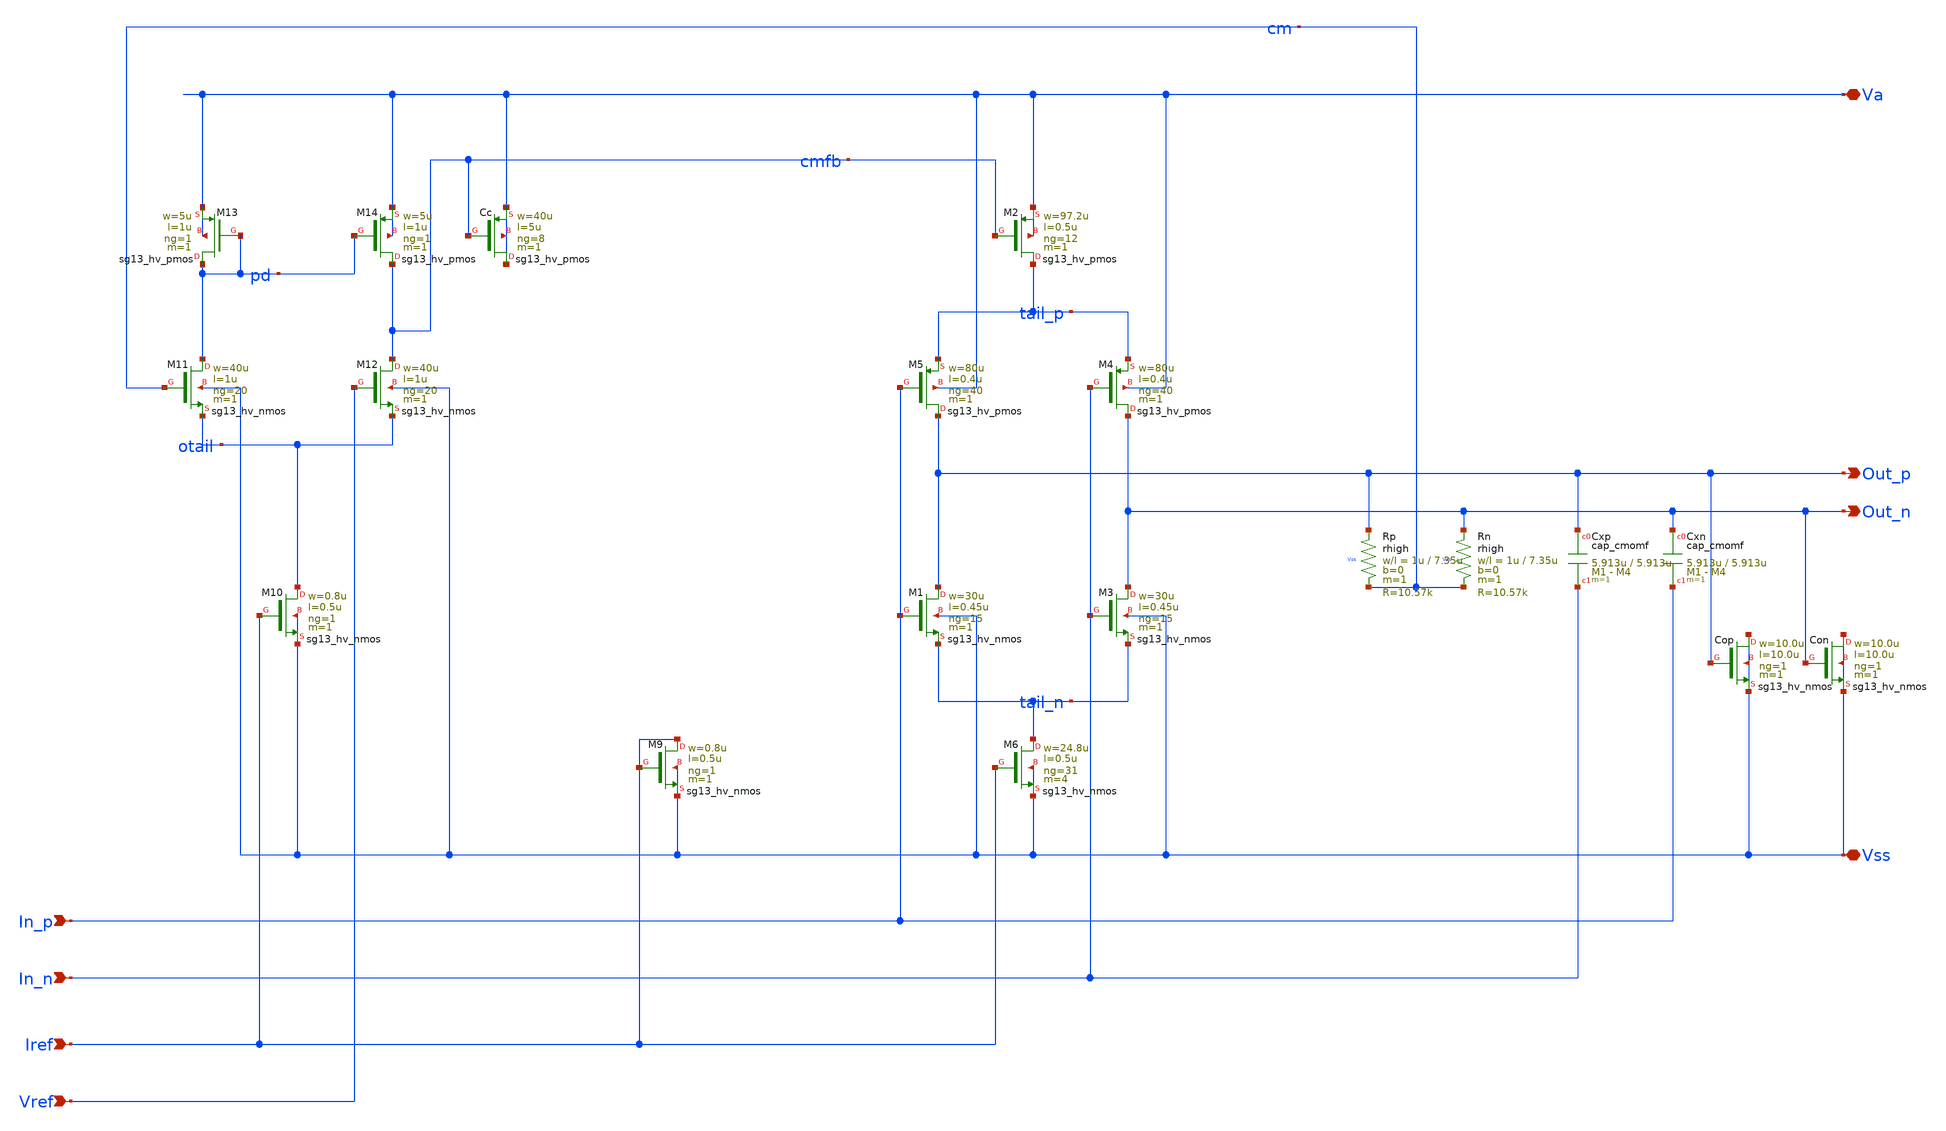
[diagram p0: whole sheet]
** sch_path: macros/lvds_tx/schematic/xschem/Driver.sch
**.subckt Driver Va Vss Out_p Out_n In_p In_n Iref Vref
*.iopin Va
*.iopin Vss
*.opin Out_p
*.opin Out_n
*.ipin In_p
*.ipin In_n
*.ipin Iref
*.ipin Vref
XM2 tail_p cmfb Va Va sg13_hv_pmos w=97.2u l=0.5u ng=12 m=1 mm_ok=1
XM5 Out_p In_p tail_p Va sg13_hv_pmos w=80u l=0.4u ng=40 m=1 mm_ok=1
XM4 Out_n In_n tail_p Va sg13_hv_pmos w=80u l=0.4u ng=40 m=1 mm_ok=1
XM1 Out_p In_p tail_n Vss sg13_hv_nmos w=30u l=0.45u ng=15 m=1 mm_ok=1
XM3 Out_n In_n tail_n Vss sg13_hv_nmos w=30u l=0.45u ng=15 m=1 mm_ok=1
XM6 tail_n Iref Vss Vss sg13_hv_nmos w=24.8u l=0.5u ng=31 m=4 mm_ok=1
XM9 Iref Iref Vss Vss sg13_hv_nmos w=0.8u l=0.5u ng=1 m=1 mm_ok=1
XM13 pd pd Va Va sg13_hv_pmos w=5u l=1u ng=1 m=1 mm_ok=1
XM14 cmfb pd Va Va sg13_hv_pmos w=5u l=1u ng=1 m=1 mm_ok=1
XM11 pd cm otail Vss sg13_hv_nmos w=40u l=1u ng=20 m=1 mm_ok=1
XM12 cmfb Vref otail Vss sg13_hv_nmos w=40u l=1u ng=20 m=1 mm_ok=1
XM10 otail Iref Vss Vss sg13_hv_nmos w=0.8u l=0.5u ng=1 m=1 mm_ok=1
XCc Va cmfb Va Va sg13_hv_pmos w=40u l=5u ng=8 m=1 mm_ok=1
XRp Out_p cm Vss rhigh w=1u l=7.35u m=1 b=0 mm_ok=1
XRn Out_n cm Vss rhigh w=1u l=7.35u m=1 b=0 mm_ok=1
XCxp Out_p In_n cap_cmomf w=5.913u l=5.913u mmin=1 mmax=4 subblock=0 rfmodel=0 subscale=1 m=1
+ mm_ok=1
XCxn Out_n In_p cap_cmomf w=5.913u l=5.913u mmin=1 mmax=4 subblock=0 rfmodel=0 subscale=1 m=1
+ mm_ok=1
XCop Vss Out_p Vss Vss sg13_hv_nmos w=10.0u l=10.0u ng=1 m=1 mm_ok=1
XCon Vss Out_n Vss Vss sg13_hv_nmos w=10.0u l=10.0u ng=1 m=1 mm_ok=1
**.ends
.end
